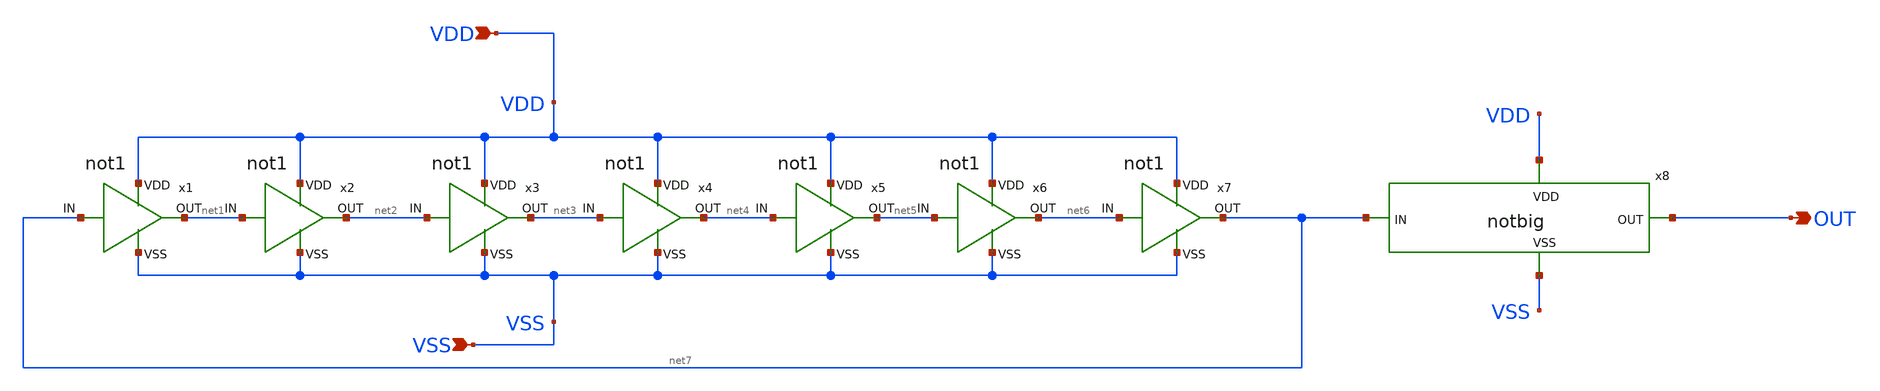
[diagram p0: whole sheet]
** sch_path: custom_gds/tt_um_alexjaeger_ringoscillator/xschem/ringosc.sch
**.subckt ringosc VDD VSS OUT
*.ipin VDD
*.ipin VSS
*.opin OUT
x1 VDD VSS net7 net1 not1
x2 VDD VSS net1 net2 not1
x3 VDD VSS net2 net3 not1
x4 VDD VSS net3 net4 not1
x5 VDD VSS net4 net5 not1
x6 VDD VSS net5 net6 not1
x7 VDD VSS net6 net7 not1
x8 VDD VSS net7 OUT notbig
**.ends

* expanding   symbol:  not1.sym # of pins=4
** sym_path: custom_gds/tt_um_alexjaeger_ringoscillator/xschem/not1.sym
** sch_path: custom_gds/tt_um_alexjaeger_ringoscillator/xschem/not1.sch
.subckt not1 VDD VSS IN OUT
*.opin OUT
*.ipin IN
*.ipin VDD
*.ipin VSS
XM1 OUT IN VSS VSS sky130_fd_pr__nfet_01v8 L=5 W=3 nf=1 ad='int((nf+1)/2) * W/nf * 0.29' as='int((nf+2)/2) * W/nf * 0.29'
+ pd='2*int((nf+1)/2) * (W/nf + 0.29)' ps='2*int((nf+2)/2) * (W/nf + 0.29)' nrd='0.29 / W' nrs='0.29 / W'
+ sa=0 sb=0 sd=0 mult=1 m=1
XM2 OUT IN VDD VDD sky130_fd_pr__pfet_01v8 L=5 W=3 nf=1 ad='int((nf+1)/2) * W/nf * 0.29' as='int((nf+2)/2) * W/nf * 0.29'
+ pd='2*int((nf+1)/2) * (W/nf + 0.29)' ps='2*int((nf+2)/2) * (W/nf + 0.29)' nrd='0.29 / W' nrs='0.29 / W'
+ sa=0 sb=0 sd=0 mult=1 m=1
.ends


* expanding   symbol:  notbig.sym # of pins=4
** sym_path: custom_gds/tt_um_alexjaeger_ringoscillator/xschem/notbig.sym
** sch_path: custom_gds/tt_um_alexjaeger_ringoscillator/xschem/notbig.sch
.subckt notbig VDD VSS IN OUT
*.opin OUT
*.ipin IN
*.ipin VDD
*.ipin VSS
XM1 OUT IN VSS VSS sky130_fd_pr__nfet_01v8 L=1 W=5 nf=1 ad='int((nf+1)/2) * W/nf * 0.29' as='int((nf+2)/2) * W/nf * 0.29'
+ pd='2*int((nf+1)/2) * (W/nf + 0.29)' ps='2*int((nf+2)/2) * (W/nf + 0.29)' nrd='0.29 / W' nrs='0.29 / W'
+ sa=0 sb=0 sd=0 mult=1 m=1
XM2 OUT IN VDD VDD sky130_fd_pr__pfet_01v8 L=1 W=5 nf=1 ad='int((nf+1)/2) * W/nf * 0.29' as='int((nf+2)/2) * W/nf * 0.29'
+ pd='2*int((nf+1)/2) * (W/nf + 0.29)' ps='2*int((nf+2)/2) * (W/nf + 0.29)' nrd='0.29 / W' nrs='0.29 / W'
+ sa=0 sb=0 sd=0 mult=1 m=1
.ends

.end
